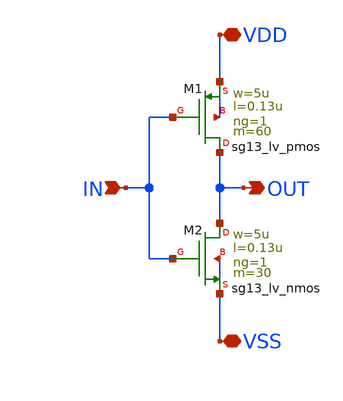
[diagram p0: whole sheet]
** sch_path: SSDOR_1V_v1/components/trans_gate_low/tg_low_inverter.sch
**.subckt tg_low_inverter VSS VDD IN OUT
*.iopin VSS
*.iopin VDD
*.ipin IN
*.opin OUT
XM1 OUT IN VDD VDD sg13_lv_pmos w=5u l=0.13u ng=1 m=60 mm_ok=1
XM2 OUT IN VSS VSS sg13_lv_nmos w=5u l=0.13u ng=1 m=30 mm_ok=1
**.ends
.end
